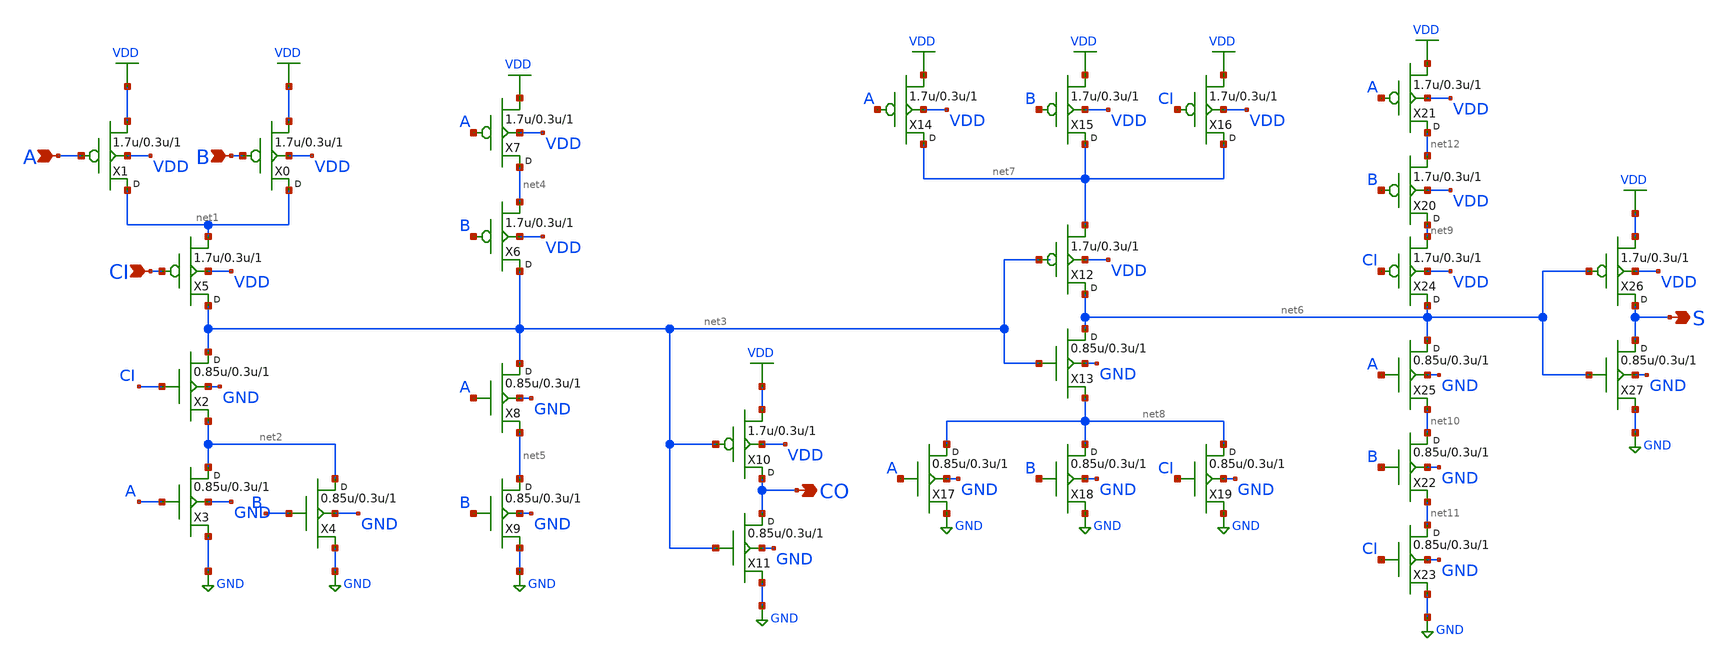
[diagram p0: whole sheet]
** sch_path: gf180mcu_osu_sc_gp9t3v3/cells/addf/gf180mcu_osu_sc_gp9t3v3__addf_1.sch
**.subckt gf180mcu_osu_sc_gp9t3v3__addf_1 A B CI S CO
*.ipin A
*.ipin B
*.ipin CI
*.opin S
*.opin CO
X1 net1 A VDD VDD pfet_03p3 w=1.7u l=0.3u m=1
X0 net1 B VDD VDD pfet_03p3 w=1.7u l=0.3u m=1
X2 net3 CI net2 GND nfet_03p3 w=0.85u l=0.3u m=1
X3 net2 A GND GND nfet_03p3 w=0.85u l=0.3u m=1
X4 net2 B GND GND nfet_03p3 w=0.85u l=0.3u m=1
X5 net3 CI net1 VDD pfet_03p3 w=1.7u l=0.3u m=1
X6 net3 B net4 VDD pfet_03p3 w=1.7u l=0.3u m=1
X7 net4 A VDD VDD pfet_03p3 w=1.7u l=0.3u m=1
X8 net3 A net5 GND nfet_03p3 w=0.85u l=0.3u m=1
X9 net5 B GND GND nfet_03p3 w=0.85u l=0.3u m=1
X10 CO net3 VDD VDD pfet_03p3 w=1.7u l=0.3u m=1
X11 CO net3 GND GND nfet_03p3 w=0.85u l=0.3u m=1
X12 net6 net3 net7 VDD pfet_03p3 w=1.7u l=0.3u m=1
X13 net6 net3 net8 GND nfet_03p3 w=0.85u l=0.3u m=1
X14 net7 A VDD VDD pfet_03p3 w=1.7u l=0.3u m=1
X15 net7 B VDD VDD pfet_03p3 w=1.7u l=0.3u m=1
X16 net7 CI VDD VDD pfet_03p3 w=1.7u l=0.3u m=1
X17 net8 A GND GND nfet_03p3 w=0.85u l=0.3u m=1
X18 net8 B GND GND nfet_03p3 w=0.85u l=0.3u m=1
X19 net8 CI GND GND nfet_03p3 w=0.85u l=0.3u m=1
X20 net9 B net12 VDD pfet_03p3 w=1.7u l=0.3u m=1
X21 net12 A VDD VDD pfet_03p3 w=1.7u l=0.3u m=1
X22 net10 B net11 GND nfet_03p3 w=0.85u l=0.3u m=1
X23 net11 CI GND GND nfet_03p3 w=0.85u l=0.3u m=1
X24 net6 CI net9 VDD pfet_03p3 w=1.7u l=0.3u m=1
X25 net6 A net10 GND nfet_03p3 w=0.85u l=0.3u m=1
X26 S net6 VDD VDD pfet_03p3 w=1.7u l=0.3u m=1
X27 S net6 GND GND nfet_03p3 w=0.85u l=0.3u m=1
**.ends
.GLOBAL VDD
.GLOBAL GND
.end
